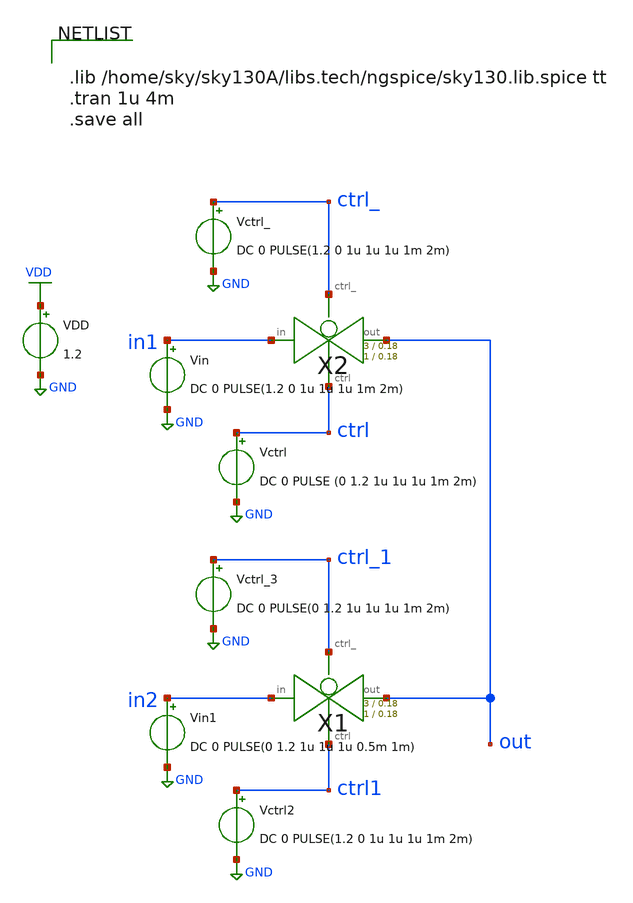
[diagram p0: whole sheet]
** sch_path: xschem/readout/switch_test.sch
**.subckt switch_test
Vin in1 GND DC 0 PULSE(1.2 0 1u 1u 1u 1m 2m)
VDD VDD GND 1.2
Vctrl ctrl GND DC 0 PULSE (0 1.2 1u 1u 1u 1m 2m)
Vctrl_ ctrl_ GND DC 0 PULSE(1.2 0 1u 1u 1u 1m 2m)
X2 in1 out ctrl_ ctrl transmission_gate Wpmos=3 Lpmos=0.18 Wnmos=1 Lnmos=0.18
Vin1 in2 GND DC 0 PULSE(0 1.2 1u 1u 1u 0.5m 1m)
Vctrl2 ctrl1 GND DC 0 PULSE(1.2 0 1u 1u 1u 1m 2m)
Vctrl_3 ctrl_1 GND DC 0 PULSE(0 1.2 1u 1u 1u 1m 2m)
X1 in2 out ctrl_1 ctrl1 transmission_gate Wpmos=3 Lpmos=0.18 Wnmos=1 Lnmos=0.18
**** begin user architecture code


.lib /home/sky/sky130A/libs.tech/ngspice/sky130.lib.spice tt
.tran 1u 4m
.save all


**** end user architecture code
**.ends

* expanding   symbol:  transmission_gate/transmission_gate.sym # of pins=4
** sym_path: xschem/transmission_gate/transmission_gate.sym
** sch_path: xschem/transmission_gate/transmission_gate.sch
.subckt transmission_gate in out ctrl_ ctrl  Wpmos=0.42 Lpmos=0.18 Wnmos=0.42 Lnmos=0.18
*.iopin in
*.iopin out
*.ipin ctrl_
*.ipin ctrl
XM1 out ctrl in GND sky130_fd_pr__nfet_01v8 L=Lnmos W=Wnmos nf=1 ad='int((nf+1)/2) * W/nf * 0.29' as='int((nf+2)/2) * W/nf * 0.29'
+ pd='2*int((nf+1)/2) * (W/nf + 0.29)' ps='2*int((nf+2)/2) * (W/nf + 0.29)' nrd='0.29 / W' nrs='0.29 / W'
+ sa=0 sb=0 sd=0 mult=1 m=1
XM2 out ctrl_ in VDD sky130_fd_pr__pfet_01v8 L=Lpmos W=Wpmos nf=1 ad='int((nf+1)/2) * W/nf * 0.29' as='int((nf+2)/2) * W/nf * 0.29'
+ pd='2*int((nf+1)/2) * (W/nf + 0.29)' ps='2*int((nf+2)/2) * (W/nf + 0.29)' nrd='0.29 / W' nrs='0.29 / W'
+ sa=0 sb=0 sd=0 mult=1 m=1
.ends

.GLOBAL VDD
.GLOBAL GND
.end
